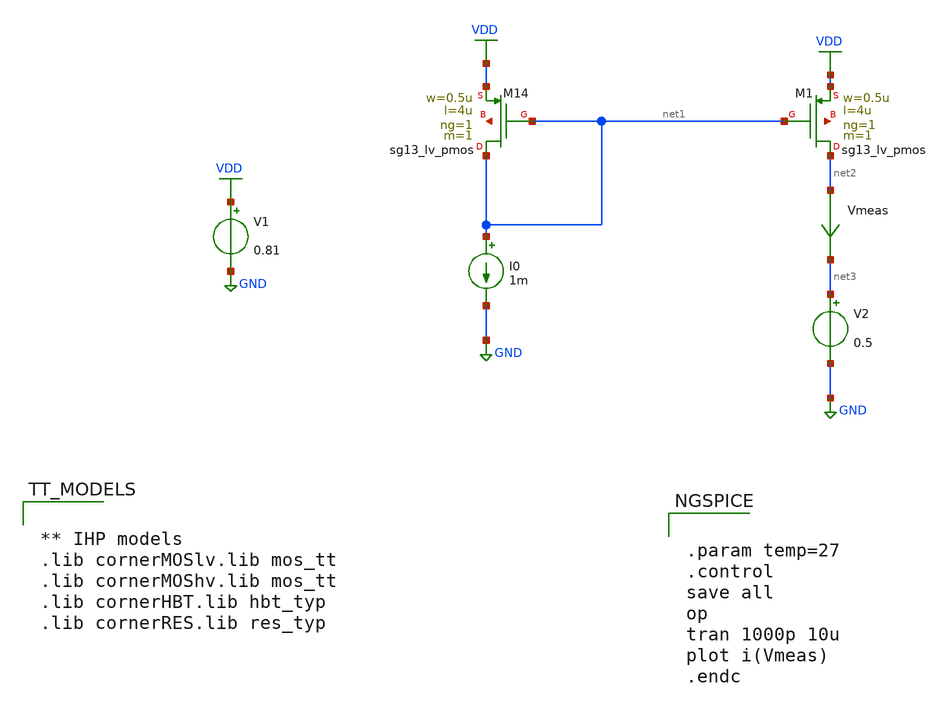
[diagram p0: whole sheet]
** sch_path: SSDOR_w_startup_1V_ihp/Ib_4u/CTAT_PTAT/untitled.sch
**.subckt untitled
V1 VDD GND 0.81
XM14 net1 net1 VDD net4 sg13_lv_pmos w=0.5u l=4u ng=1 m=1 mm_ok=1
I0 net1 GND 1m
XM1 net2 net1 VDD net5 sg13_lv_pmos w=0.5u l=4u ng=1 m=1 mm_ok=1
V2 net3 GND 0.5
Vmeas net2 net3 0
.save i(vmeas)
**** begin user architecture code


** IHP models
.lib cornerMOSlv.lib mos_tt
.lib cornerMOShv.lib mos_tt
.lib cornerHBT.lib hbt_typ
.lib cornerRES.lib res_typ




.param temp=27
.control
save all
op
tran 1000p 10u
plot i(Vmeas)
.endc


**** end user architecture code
**.ends
.GLOBAL VDD
.GLOBAL GND
.end
